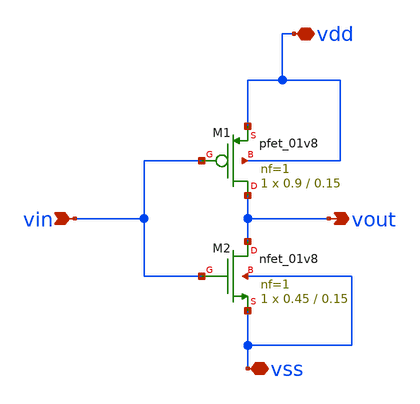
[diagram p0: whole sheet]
** sch_path: designs/libs/snn_analog/encoder/sch/tut1_xsc.sch
**.subckt tut1_xsc vout vin vdd vss
*.opin vout
*.ipin vin
*.iopin vdd
*.iopin vss
XM1 vout vin vdd vdd sky130_fd_pr__pfet_01v8 L=0.15 W=0.9 nf=1 ad='int((nf+1)/2) * W/nf * 0.29' as='int((nf+2)/2) * W/nf * 0.29'
+ pd='2*int((nf+1)/2) * (W/nf + 0.29)' ps='2*int((nf+2)/2) * (W/nf + 0.29)' nrd='0.29 / W' nrs='0.29 / W'
+ sa=0 sb=0 sd=0 mult=1 m=1
XM2 vout vin vss vss sky130_fd_pr__nfet_01v8 L=0.15 W=0.45 nf=1 ad='int((nf+1)/2) * W/nf * 0.29' as='int((nf+2)/2) * W/nf * 0.29'
+ pd='2*int((nf+1)/2) * (W/nf + 0.29)' ps='2*int((nf+2)/2) * (W/nf + 0.29)' nrd='0.29 / W' nrs='0.29 / W'
+ sa=0 sb=0 sd=0 mult=1 m=1
**.ends
.end
